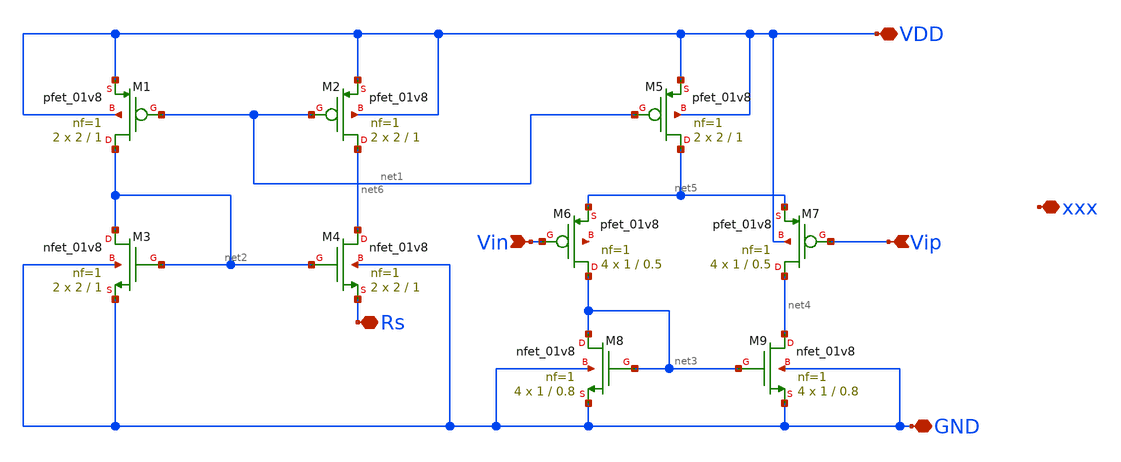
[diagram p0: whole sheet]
** sch_path: op-amp.sch
**.subckt op-amp VDD xxx GND Rs Vip Vin
*.iopin VDD
*.iopin xxx
*.iopin GND
*.iopin Rs
*.ipin Vip
*.ipin Vin
XM1 net2 net1 VDD VDD sky130_fd_pr__pfet_01v8 L=1 W=2 nf=1 ad='int((nf+1)/2) * W/nf * 0.29' as='int((nf+2)/2) * W/nf * 0.29'
+ pd='2*int((nf+1)/2) * (W/nf + 0.29)' ps='2*int((nf+2)/2) * (W/nf + 0.29)' nrd='0.29 / W' nrs='0.29 / W'
+ sa=0 sb=0 sd=0 mult=2 m=2
XM2 net6 net1 VDD VDD sky130_fd_pr__pfet_01v8 L=1 W=2 nf=1 ad='int((nf+1)/2) * W/nf * 0.29' as='int((nf+2)/2) * W/nf * 0.29'
+ pd='2*int((nf+1)/2) * (W/nf + 0.29)' ps='2*int((nf+2)/2) * (W/nf + 0.29)' nrd='0.29 / W' nrs='0.29 / W'
+ sa=0 sb=0 sd=0 mult=2 m=2
XM3 net2 net2 GND GND sky130_fd_pr__nfet_01v8 L=1 W=2 nf=1 ad='int((nf+1)/2) * W/nf * 0.29' as='int((nf+2)/2) * W/nf * 0.29'
+ pd='2*int((nf+1)/2) * (W/nf + 0.29)' ps='2*int((nf+2)/2) * (W/nf + 0.29)' nrd='0.29 / W' nrs='0.29 / W'
+ sa=0 sb=0 sd=0 mult=2 m=2
XM4 net6 net2 Rs GND sky130_fd_pr__nfet_01v8 L=1 W=2 nf=1 ad='int((nf+1)/2) * W/nf * 0.29' as='int((nf+2)/2) * W/nf * 0.29'
+ pd='2*int((nf+1)/2) * (W/nf + 0.29)' ps='2*int((nf+2)/2) * (W/nf + 0.29)' nrd='0.29 / W' nrs='0.29 / W'
+ sa=0 sb=0 sd=0 mult=2 m=2
XM5 net5 net1 VDD VDD sky130_fd_pr__pfet_01v8 L=1 W=2 nf=1 ad='int((nf+1)/2) * W/nf * 0.29' as='int((nf+2)/2) * W/nf * 0.29'
+ pd='2*int((nf+1)/2) * (W/nf + 0.29)' ps='2*int((nf+2)/2) * (W/nf + 0.29)' nrd='0.29 / W' nrs='0.29 / W'
+ sa=0 sb=0 sd=0 mult=2 m=2
XM6 net3 Vin net5 net7 sky130_fd_pr__pfet_01v8 L=0.5 W=1 nf=1 ad='int((nf+1)/2) * W/nf * 0.29' as='int((nf+2)/2) * W/nf * 0.29'
+ pd='2*int((nf+1)/2) * (W/nf + 0.29)' ps='2*int((nf+2)/2) * (W/nf + 0.29)' nrd='0.29 / W' nrs='0.29 / W'
+ sa=0 sb=0 sd=0 mult=4 m=4
XM7 net4 Vip net5 VDD sky130_fd_pr__pfet_01v8 L=0.5 W=1 nf=1 ad='int((nf+1)/2) * W/nf * 0.29' as='int((nf+2)/2) * W/nf * 0.29'
+ pd='2*int((nf+1)/2) * (W/nf + 0.29)' ps='2*int((nf+2)/2) * (W/nf + 0.29)' nrd='0.29 / W' nrs='0.29 / W'
+ sa=0 sb=0 sd=0 mult=4 m=4
XM8 net3 net3 GND GND sky130_fd_pr__nfet_01v8 L=0.8 W=1 nf=1 ad='int((nf+1)/2) * W/nf * 0.29' as='int((nf+2)/2) * W/nf * 0.29'
+ pd='2*int((nf+1)/2) * (W/nf + 0.29)' ps='2*int((nf+2)/2) * (W/nf + 0.29)' nrd='0.29 / W' nrs='0.29 / W'
+ sa=0 sb=0 sd=0 mult=4 m=4
XM9 net4 net3 GND GND sky130_fd_pr__nfet_01v8 L=0.8 W=1 nf=1 ad='int((nf+1)/2) * W/nf * 0.29' as='int((nf+2)/2) * W/nf * 0.29'
+ pd='2*int((nf+1)/2) * (W/nf + 0.29)' ps='2*int((nf+2)/2) * (W/nf + 0.29)' nrd='0.29 / W' nrs='0.29 / W'
+ sa=0 sb=0 sd=0 mult=4 m=4
**.ends
.end
